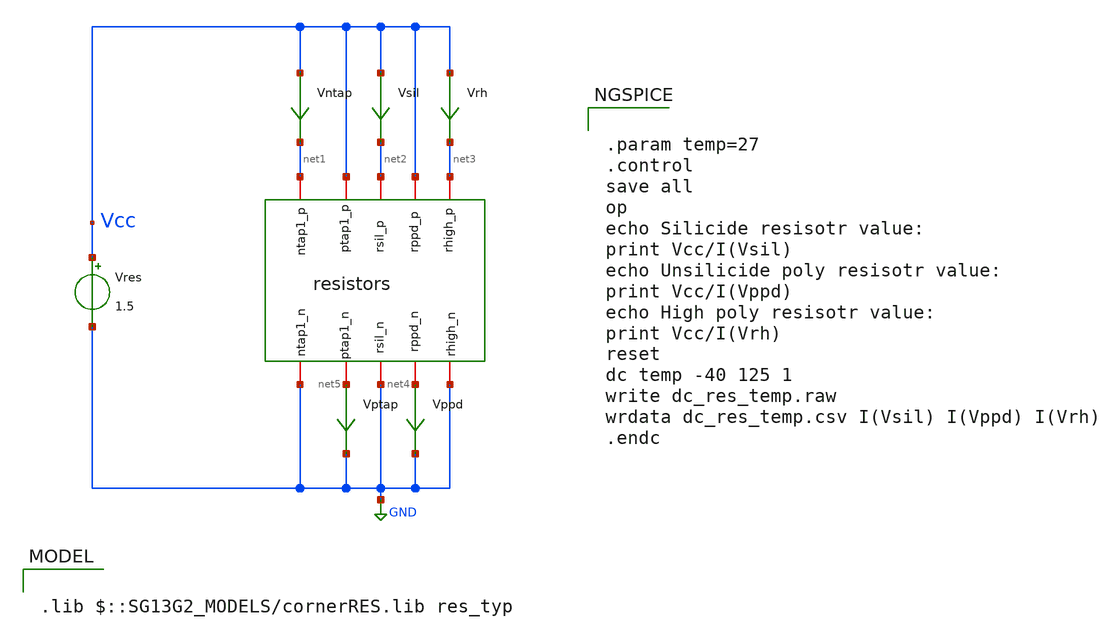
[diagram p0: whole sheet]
** sch_path: ts_pr_May2024/design_data/xschem/resistors_tb.sch
* Copyright 2023 IHP PDK Authors
**.subckt resistors_tb
Vres Vcc GND 1.5
Vsil Vcc net2 0
.save i(vsil)
Vppd net4 GND 0
.save i(vppd)
Vrh Vcc net3 0
.save i(vrh)
Vptap net5 GND 0
.save i(vptap)
Vntap Vcc net1 0
.save i(vntap)
x1 Vcc net1 net3 Vcc net2 net5 GND net4 GND GND resistors
**** begin user architecture code

.lib $::SG13G2_MODELS/cornerRES.lib res_typ



.param temp=27
.control
save all
op
echo Silicide resisotr value:
print Vcc/I(Vsil)
echo Unsilicide poly resisotr value:
print Vcc/I(Vppd)
echo High poly resisotr value:
print Vcc/I(Vrh)
reset
dc temp -40 125 1
write dc_res_temp.raw
wrdata dc_res_temp.csv I(Vsil) I(Vppd) I(Vrh)
.endc


**** end user architecture code
**.ends

* expanding   symbol:  resistors.sym # of pins=10
** sym_path: ts_pr_May2024/design_data/xschem/resistors.sym
** sch_path: ts_pr_May2024/design_data/xschem/resistors.sch
.subckt resistors rppd_p ntap1_p rhigh_p ptap1_p rsil_p ptap1_n rhigh_n rppd_n rsil_n ntap1_n
*.iopin ntap1_p
*.iopin ptap1_p
*.iopin rsil_p
*.iopin rppd_p
*.iopin rhigh_p
*.iopin ntap1_n
*.iopin ptap1_n
*.iopin rsil_n
*.iopin rppd_n
*.iopin rhigh_n
XR2 rppd_p rppd_n sub! rppd w=0.5e-6 l=2.5e-6 m=1 b=0 mm_ok=1
XR3 rhigh_p rhigh_n sub! rhigh w=0.5e-6 l=2.0e-6 m=1 b=0 mm_ok=1
XR1 rsil_p rsil_n sub! rsil w=0.5e-5 l=0.5e-5 m=1 mm_ok=1
XR4 ptap1_p ptap1_n ptap1 R=262.8 w=0.78e-6 l=0.78e-6
XR5 ntap1_p ntap1_n ntap1 R=262.8 w=0.78e-6 l=0.78e-6
.ends

.GLOBAL GND
.end
